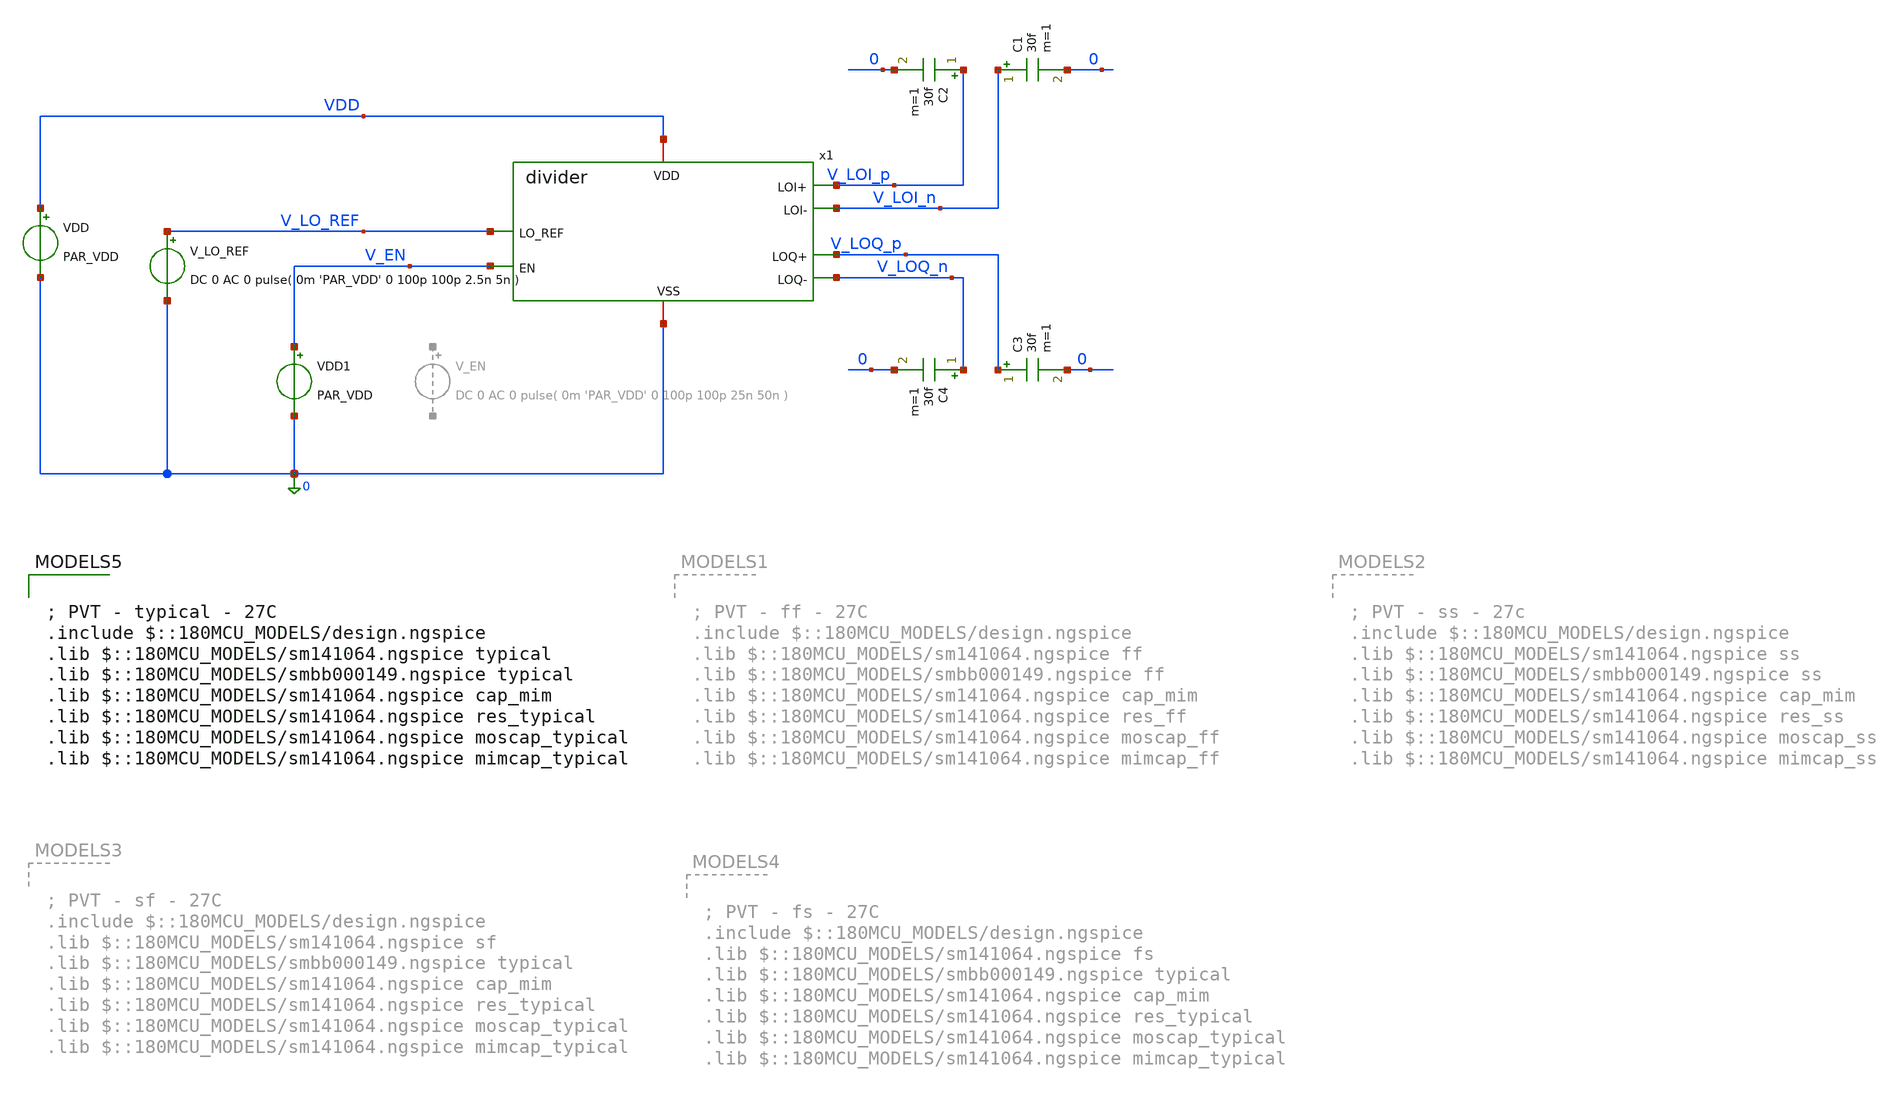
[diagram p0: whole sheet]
** sch_path: designs/divider/testbench/tb_divider_pvt.sch
**.subckt tb_divider_pvt
VDD VDD 0 PAR_VDD
V_LO_REF V_LO_REF 0 DC 0 AC 0 pulse( 0m 'PAR_VDD' 0 100p 100p 2.5n 5n )
C1 V_LOI_n 0 30f m=1
C2 V_LOI_p 0 30f m=1
C3 V_LOQ_p 0 30f m=1
C4 V_LOQ_n 0 30f m=1
VDD1 V_EN 0 PAR_VDD
x1 VDD 0 V_LO_REF V_LOI_p V_LOI_n V_LOQ_p V_LOQ_n V_EN divider
**** begin user architecture code


** PARAMS

.PARAM PAR_VDD=3.3

.control
destroy all
save all
write tb_divider.raw

op
print v(V_LOI_p) v(V_LOI_n)


;transient analysis
tran 0.1ns 1us

let V_LOI = v_loi_p - v_loi_n
let V_LOQ = v_loq_p - v_loq_n

plot v(V_LO_REF) v(V_LOI_p)+4 v(V_LOI_n)+4  v(V_LOQ_p)-4 v(V_LOQ_n)-4 xlimit 10n 20n;plot divider
+ output
plot v(V_LO_REF) V_LOI V_LOQ xlimit 10n 20n; plot differential output
;plot v(V_EN) v(x1.EN_BAR) v(x1.LO_REF_GATED) v(x1.LO_REF_BAR); plot enable signal and clock signal
+ status

plot i(vdd)*3.3 ;transient power

;plot i(v.x1.v1) plot i(v.x1.v2)
;plot v(V_LO_REF) v(x1.LO_REF_BAR)

meas tran t_diff TRIG v(V_LOI) VAL=0 TD=10n RISE=1 TARG v(V_LOQ) VAL=0 TD=10n RISE=1 ; time
+ difference between first rising 0 crossing of V_LOI and first rising 0 cross of V_LOQ after 10ns

;fft of input and output
linearize v(V_LOI) v(v_loq)
fft v(V_LOI) v(v_loq)
plot mag(v(V_LOI)) vs frequency mag(v(v_loq)) vs frequency


let V_LOI_MAG = mag(V_LOI)
let V_LOQ_MAG = mag(V_LOQ)
let V_LOI_MAX = maximum(V_LOI_MAG)-0.001; subtract small amount so that meas can find it
meas sp f_har_1 WHEN v(V_LOI_MAG)=V_LOI_MAX; measure first harmonic frequency by measuring frequency
+ of the largest voltage component

;calculate phase error with transient data
let phase_diff_transient = tran1.t_diff * f_har_1 * 360; phase difference = t_diff/t_period = t_diff
+ * f * 360 deg/1
;print phase_diff_transient


;calculate phase error with FFT
let phase_diff_fft = (cph(V_LOI)-cph(V_LOQ))*360/2/pi
meas sp phase_diff_har_1 FIND phase_diff_fft WHEN frequency=f_har_1
;print phase_diff_har_1

echo 'Phase Error with Transient (deg)'
print phase_diff_transient-90
echo 'Phase Error with FFT (deg)'
print phase_diff_har_1-90
echo 'I/Q Amplitude Error (%)'
print (maximum(V_LOQ_MAG)/maximum(V_LOI_MAG)-1)*100

.endc



; PVT - typical - 27C
.include $::180MCU_MODELS/design.ngspice
.lib $::180MCU_MODELS/sm141064.ngspice typical
.lib $::180MCU_MODELS/smbb000149.ngspice typical
.lib $::180MCU_MODELS/sm141064.ngspice cap_mim
.lib $::180MCU_MODELS/sm141064.ngspice res_typical
.lib $::180MCU_MODELS/sm141064.ngspice moscap_typical
.lib $::180MCU_MODELS/sm141064.ngspice mimcap_typical

**** end user architecture code
**.ends
.end
